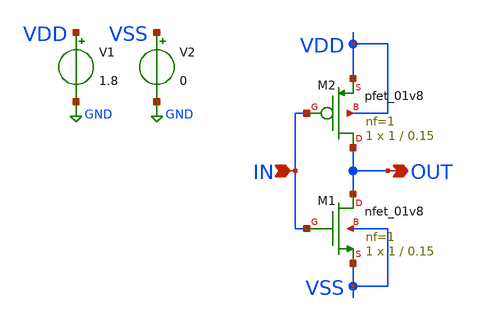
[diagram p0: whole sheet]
** sch_path: hgu/xschem/inv.sch
**.subckt inv OUT IN
*.opin OUT
*.ipin IN
XM1 OUT IN VSS VSS sky130_fd_pr__nfet_01v8 L=0.15 W=1 nf=1 ad='int((nf+1)/2) * W/nf * 0.29' as='int((nf+2)/2) * W/nf * 0.29'
+ pd='2*int((nf+1)/2) * (W/nf + 0.29)' ps='2*int((nf+2)/2) * (W/nf + 0.29)' nrd='0.29 / W' nrs='0.29 / W'
+ sa=0 sb=0 sd=0 mult=1 m=1
XM2 OUT IN VDD VDD sky130_fd_pr__pfet_01v8 L=0.15 W=1 nf=1 ad='int((nf+1)/2) * W/nf * 0.29' as='int((nf+2)/2) * W/nf * 0.29'
+ pd='2*int((nf+1)/2) * (W/nf + 0.29)' ps='2*int((nf+2)/2) * (W/nf + 0.29)' nrd='0.29 / W' nrs='0.29 / W'
+ sa=0 sb=0 sd=0 mult=1 m=1
V1 VDD GND 1.8
V2 VSS GND 0
**.ends
.GLOBAL GND
.end
